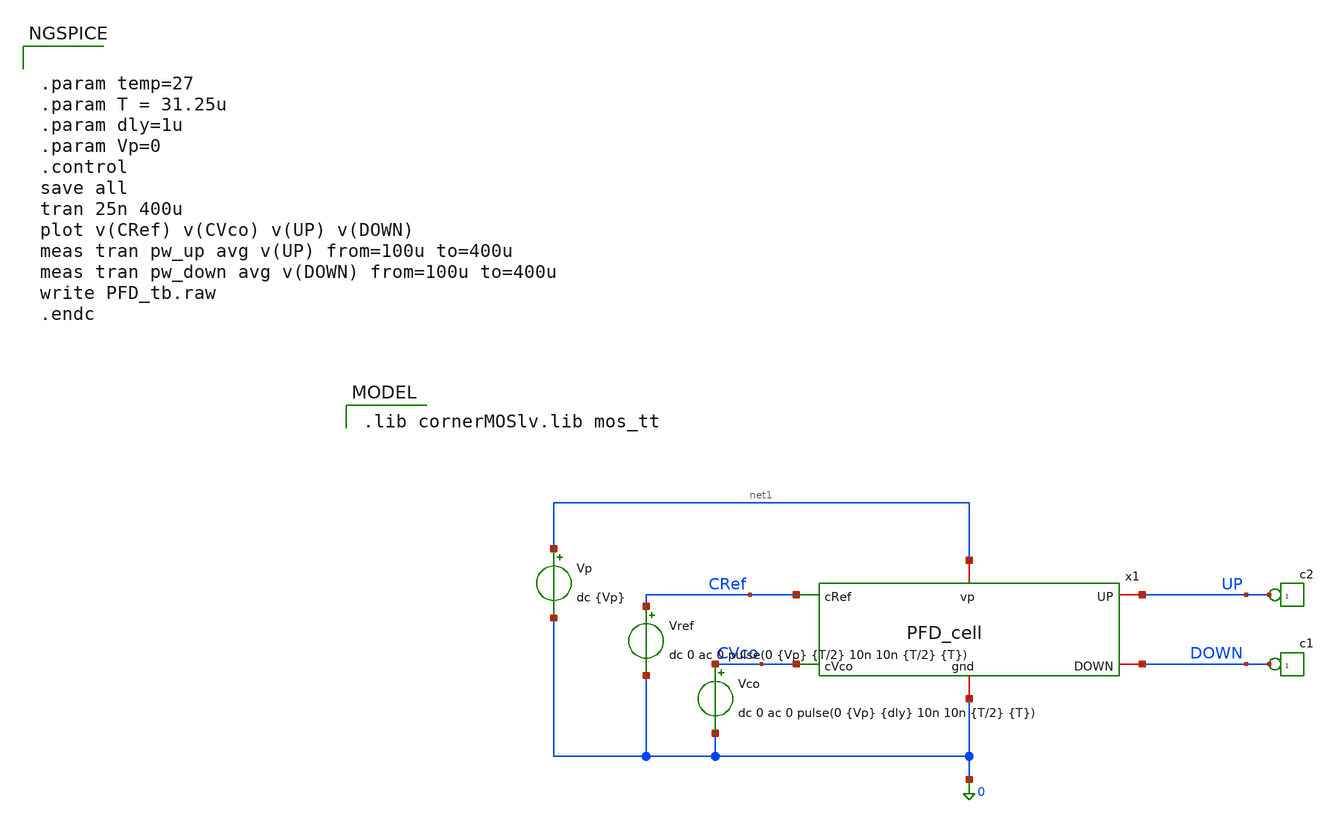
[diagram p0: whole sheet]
** sch_path: PFD/PFD_tb.sch
**.subckt PFD_tb
x1 0 net1 CRef UP DOWN CVco PFD_cell
*connector(1,1) ?1 DOWN
*connector(1,1) ?1 UP
Vref CRef 0 dc 0 ac 0 pulse(0 {Vp} {T/2} 10n 10n {T/2} {T})
Vco CVco 0 dc 0 ac 0 pulse(0 {Vp} {dly} 10n 10n {T/2} {T})
Vp net1 0 dc {Vp}
**** begin user architecture code
 .lib cornerMOSlv.lib mos_tt



.param temp=27
.param T = 31.25u
.param dly=1u
.param Vp=0
.control
save all
tran 25n 400u
plot v(CRef) v(CVco) v(UP) v(DOWN)
meas tran pw_up avg v(UP) from=100u to=400u
meas tran pw_down avg v(DOWN) from=100u to=400u
write PFD_tb.raw
.endc


**** end user architecture code
**.ends
.end
